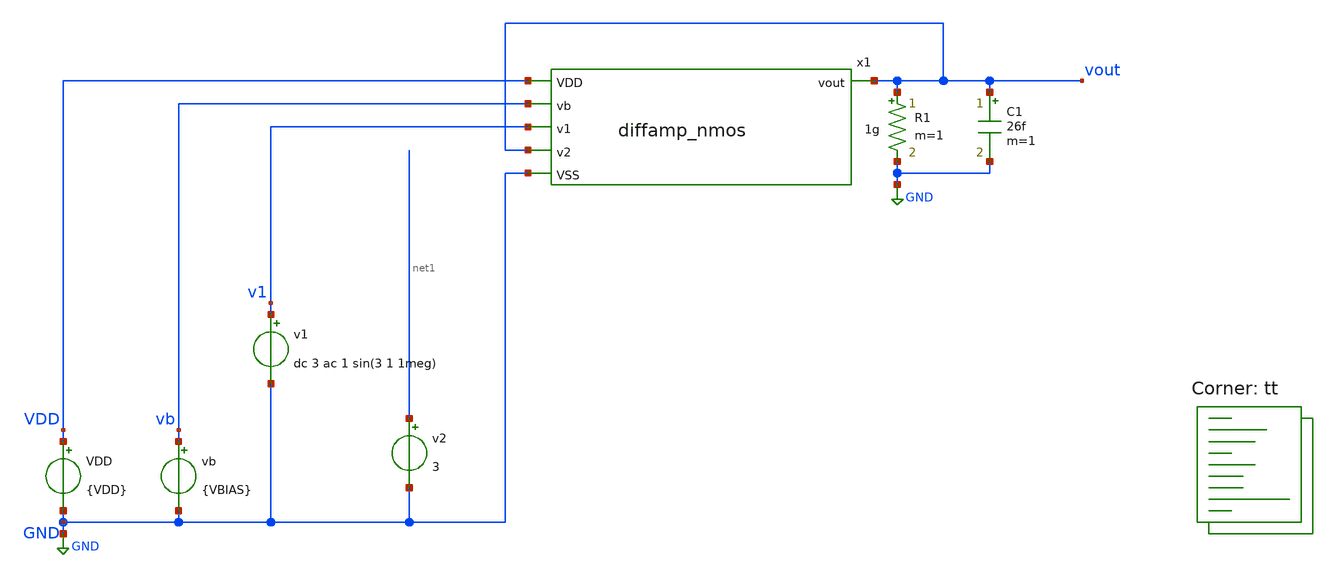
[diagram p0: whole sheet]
** sch_path: xschem/tb_diffamp_nmos_ac.sch
**.subckt tb_diffamp_nmos_ac
x1 v1 vout GND VDD vb vout diffamp_nmos
VDD VDD GND {VDD}
vb vb GND {VBIAS}
v1 v1 GND dc 3 ac 1 sin(3 1 1meg)
R1 vout GND 1g m=1
v2 net1 GND 3
C1 vout GND 26f m=1
**** begin user architecture code
.lib $::SKYWATER_MODELS/sky130.lib.spice tt



.options reltol=0.0001 abstol=10e-15
.include diffamp_nmos.spice
.param VDD=5
.param VSS=0
.param VBIAS=1
.options savecurrents
* .options reltol=0.01 abstol=10e-12
.control
  save all
  op
  remzerovec
  write tb_diffamp_nmos_ac.raw
  set appendwrite
  * ac sweep
  ac dec 20 1 1gig
  remzerovec
  write tb_diffamp_nmos_ac.raw
  * tran
  tran 1n 5u
  remzerovec
  write tb_diffamp_nmos_ac.raw
.endc



**** end user architecture code
**.ends
.GLOBAL GND
.end
